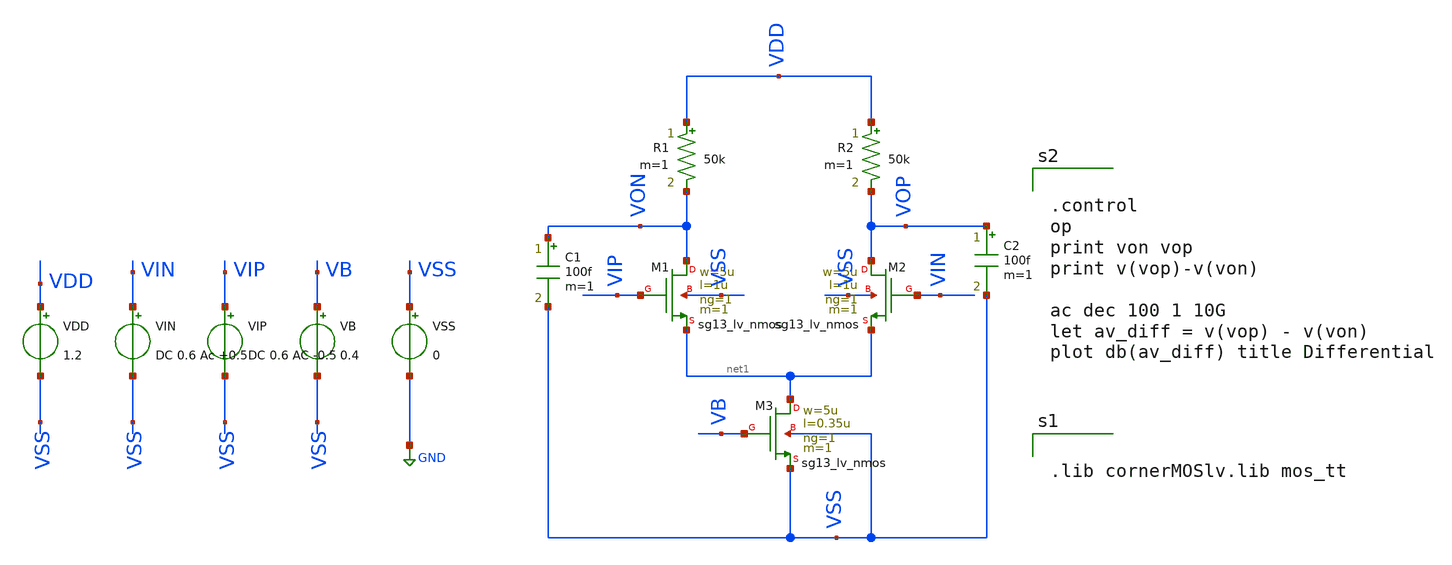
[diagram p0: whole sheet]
** sch_path: BTDay4-Ex/Ex1_Lecture4.sch
**.subckt Ex1_Lecture4
XM1 VON VIP net1 VSS sg13_lv_nmos w=5u l=1u ng=1 m=1 mm_ok=1
XM2 VOP VIN net1 VSS sg13_lv_nmos w=5u l=1u ng=1 m=1 mm_ok=1
XM3 net1 VB VSS VSS sg13_lv_nmos w=5u l=0.35u ng=1 m=1 mm_ok=1
R1 VDD VON 50k m=1
R2 VDD VOP 50k m=1
VDD VDD VSS 1.2
VIN VIN VSS DC 0.6 Ac +0.5
VIP VIP VSS DC 0.6 AC -0.5
VB VB VSS 0.4
VSS VSS GND 0
C1 VON VSS 100f m=1
C2 VOP VSS 100f m=1
**** begin user architecture code


.lib cornerMOSlv.lib mos_tt




.control
op
print von vop
print v(vop)-v(von)

ac dec 100 1 10G
let av_diff = v(vop) - v(von)
plot db(av_diff) title Differential

**** end user architecture code
**.ends
.GLOBAL GND
.end
